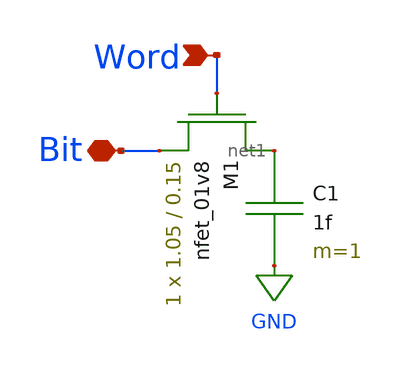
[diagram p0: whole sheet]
** sch_path: DRAM_Components/Schematic/MemoryCell1.sch
**.subckt MemoryCell1 Word Bit
*.ipin Word
*.iopin Bit
C1 net1 GND 1f m=1
XM1 net1 Word Bit VN sky130_fd_pr__nfet_01v8 L=0.15 W=1.05 nf=1 ad='int((nf+1)/2) * W/nf * 0.29' as='int((nf+2)/2) * W/nf * 0.29'
+ pd='2*int((nf+1)/2) * (W/nf + 0.29)' ps='2*int((nf+2)/2) * (W/nf + 0.29)' nrd='0.29 / W' nrs='0.29 / W'
+ sa=0 sb=0 sd=0 mult=1 m=1
**.ends
.GLOBAL GND
.end
